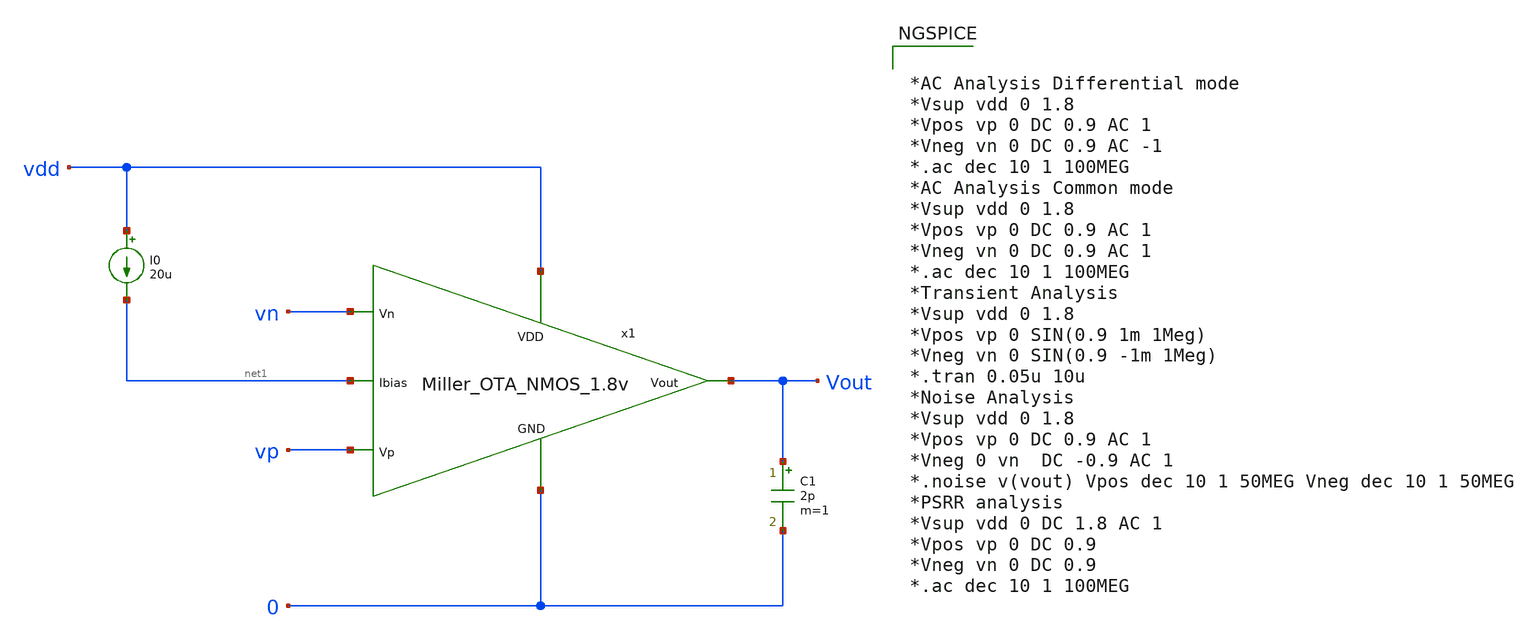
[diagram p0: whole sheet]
** sch_path: Analog_Blocks/OTA/Testbench/Miller_OTA_NMOS_1.8v_TB.sch
**.subckt Miller_OTA_NMOS_1.8v_TB
I0 vdd net1 20u
C1 Vout 0 2p m=1
x1 vdd vn vp Vout net1 0 Miller_OTA_NMOS_1.8v
**** begin user architecture code


*AC Analysis Differential mode
*Vsup vdd 0 1.8
*Vpos vp 0 DC 0.9 AC 1
*Vneg vn 0 DC 0.9 AC -1
*.ac dec 10 1 100MEG
*AC Analysis Common mode
*Vsup vdd 0 1.8
*Vpos vp 0 DC 0.9 AC 1
*Vneg vn 0 DC 0.9 AC 1
*.ac dec 10 1 100MEG
*Transient Analysis
*Vsup vdd 0 1.8
*Vpos vp 0 SIN(0.9 1m 1Meg)
*Vneg vn 0 SIN(0.9 -1m 1Meg)
*.tran 0.05u 10u
*Noise Analysis
*Vsup vdd 0 1.8
*Vpos vp 0 DC 0.9 AC 1
*Vneg 0 vn  DC -0.9 AC 1
*.noise v(vout) Vpos dec 10 1 50MEG Vneg dec 10 1 50MEG
*PSRR analysis
*Vsup vdd 0 DC 1.8 AC 1
*Vpos vp 0 DC 0.9
*Vneg vn 0 DC 0.9
*.ac dec 10 1 100MEG



.include $::SKYWATER_MODELS/cells/nfet_01v8/sky130_fd_pr__nfet_01v8__tt.corner.spice
.include $::SKYWATER_MODELS/cells/nfet_01v8_lvt/sky130_fd_pr__nfet_01v8_lvt__tt.corner.spice
.include $::SKYWATER_MODELS/cells/pfet_01v8/sky130_fd_pr__pfet_01v8__tt.corner.spice
.include $::SKYWATER_MODELS/cells/nfet_03v3_nvt/sky130_fd_pr__nfet_03v3_nvt__tt.corner.spice
.include $::SKYWATER_MODELS/cells/nfet_05v0_nvt/sky130_fd_pr__nfet_05v0_nvt__tt.corner.spice
.include $::SKYWATER_MODELS/cells/esd_nfet_01v8/sky130_fd_pr__esd_nfet_01v8__tt.corner.spice
.include $::SKYWATER_MODELS/cells/pfet_01v8_lvt/sky130_fd_pr__pfet_01v8_lvt__tt.corner.spice
.include $::SKYWATER_MODELS/cells/pfet_01v8_hvt/sky130_fd_pr__pfet_01v8_hvt__tt.corner.spice
.include $::SKYWATER_MODELS/cells/esd_pfet_g5v0d10v5/sky130_fd_pr__esd_pfet_g5v0d10v5__tt.corner.spice
.include $::SKYWATER_MODELS/cells/pfet_g5v0d10v5/sky130_fd_pr__pfet_g5v0d10v5__tt.corner.spice
.include $::SKYWATER_MODELS/cells/pfet_g5v0d16v0/sky130_fd_pr__pfet_g5v0d16v0__tt.corner.spice
.include $::SKYWATER_MODELS/cells/nfet_g5v0d10v5/sky130_fd_pr__nfet_g5v0d10v5__tt.corner.spice
.include $::SKYWATER_MODELS/cells/nfet_g5v0d16v0/sky130_fd_pr__nfet_g5v0d16v0__tt_discrete.corner.spice
.include $::SKYWATER_MODELS/cells/esd_nfet_g5v0d10v5/sky130_fd_pr__esd_nfet_g5v0d10v5__tt.corner.spice
.include $::SKYWATER_MODELS/models/corners/tt/nonfet.spice
* Mismatch parameters
.include $::SKYWATER_MODELS/cells/nfet_01v8/sky130_fd_pr__nfet_01v8__mismatch.corner.spice
.include $::SKYWATER_MODELS/cells/pfet_01v8/sky130_fd_pr__pfet_01v8__mismatch.corner.spice
.include $::SKYWATER_MODELS/cells/nfet_01v8_lvt/sky130_fd_pr__nfet_01v8_lvt__mismatch.corner.spice
.include $::SKYWATER_MODELS/cells/pfet_01v8_lvt/sky130_fd_pr__pfet_01v8_lvt__mismatch.corner.spice
.include $::SKYWATER_MODELS/cells/pfet_01v8_hvt/sky130_fd_pr__pfet_01v8_hvt__mismatch.corner.spice
.include $::SKYWATER_MODELS/cells/nfet_g5v0d10v5/sky130_fd_pr__nfet_g5v0d10v5__mismatch.corner.spice
.include $::SKYWATER_MODELS/cells/pfet_g5v0d10v5/sky130_fd_pr__pfet_g5v0d10v5__mismatch.corner.spice
.include $::SKYWATER_MODELS/cells/nfet_05v0_nvt/sky130_fd_pr__nfet_05v0_nvt__mismatch.corner.spice
.include $::SKYWATER_MODELS/cells/nfet_03v3_nvt/sky130_fd_pr__nfet_03v3_nvt__mismatch.corner.spice
* Resistor$::SKYWATER_MODELS/Capacitor
.include $::SKYWATER_MODELS/models/r+c/res_typical__cap_typical.spice
.include $::SKYWATER_MODELS/models/r+c/res_typical__cap_typical__lin.spice
* Special cells
.include $::SKYWATER_MODELS/models/corners/tt/specialized_cells.spice
* All models
.include $::SKYWATER_MODELS/models/all.spice
* Corner
.include $::SKYWATER_MODELS/models/corners/tt/rf.spice

**** end user architecture code
**.ends
.end
